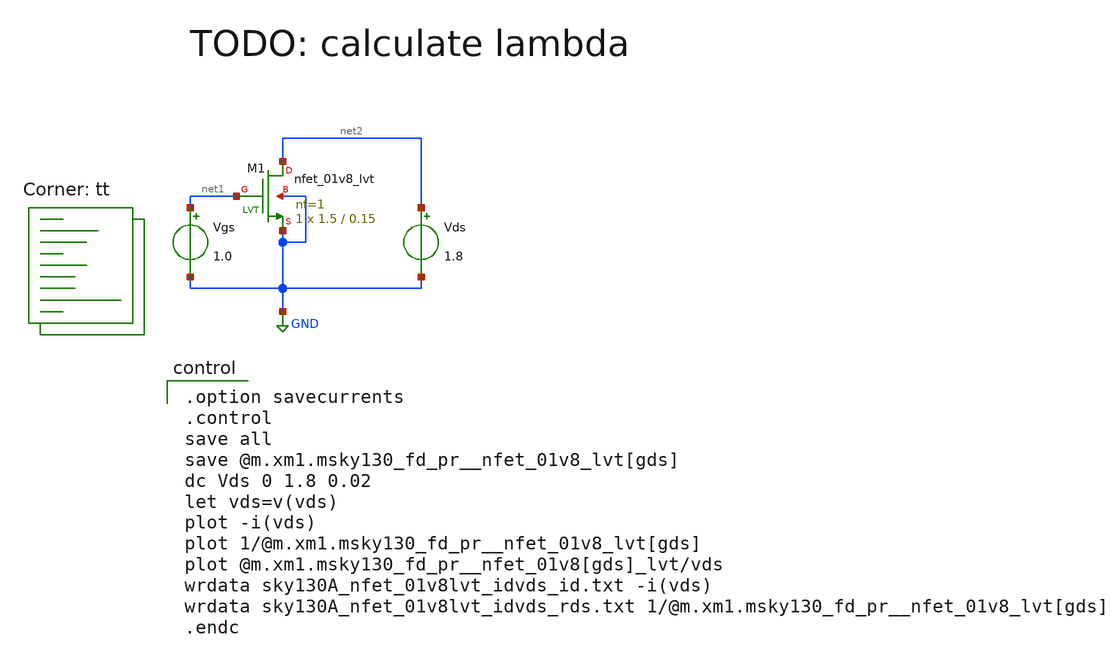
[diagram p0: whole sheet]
** sch_path: xschem/MOSFET/sky130A_nfet_01v8lvt_idvds.sch
**.subckt sky130A_nfet_01v8lvt_idvds
Vgs net1 GND 1.0
Vds net2 GND 1.8
XM1 net2 net1 GND GND sky130_fd_pr__nfet_01v8_lvt L=0.15 W=1.5 nf=1 ad='int((1 + 1)/2) * 1.5 / 1 * 0.29'
+ as='int((1 + 2)/2) * 1.5 / 1 * 0.29' pd='2*int((1 + 1)/2) * (1.5 / 1 + 0.29)' ps='2*int((1 + 2)/2) * (1.5 / 1 + 0.29)'
+ nrd='0.29 / 1.5 ' nrs='0.29 / 1.5 ' sa=0 sb=0 sd=0 mult=1 m=1
**** begin user architecture code

.option savecurrents
.control
save all
save @m.xm1.msky130_fd_pr__nfet_01v8_lvt[gds]
dc Vds 0 1.8 0.02
let vds=v(vds)
plot -i(vds)
plot 1/@m.xm1.msky130_fd_pr__nfet_01v8_lvt[gds]
plot @m.xm1.msky130_fd_pr__nfet_01v8[gds]_lvt/vds
wrdata sky130A_nfet_01v8lvt_idvds_id.txt -i(vds)
wrdata sky130A_nfet_01v8lvt_idvds_rds.txt 1/@m.xm1.msky130_fd_pr__nfet_01v8_lvt[gds]
.endc

.lib $::SKYWATER_MODELS/sky130.lib.spice tt
**** end user architecture code
**.ends
.GLOBAL GND
.end
